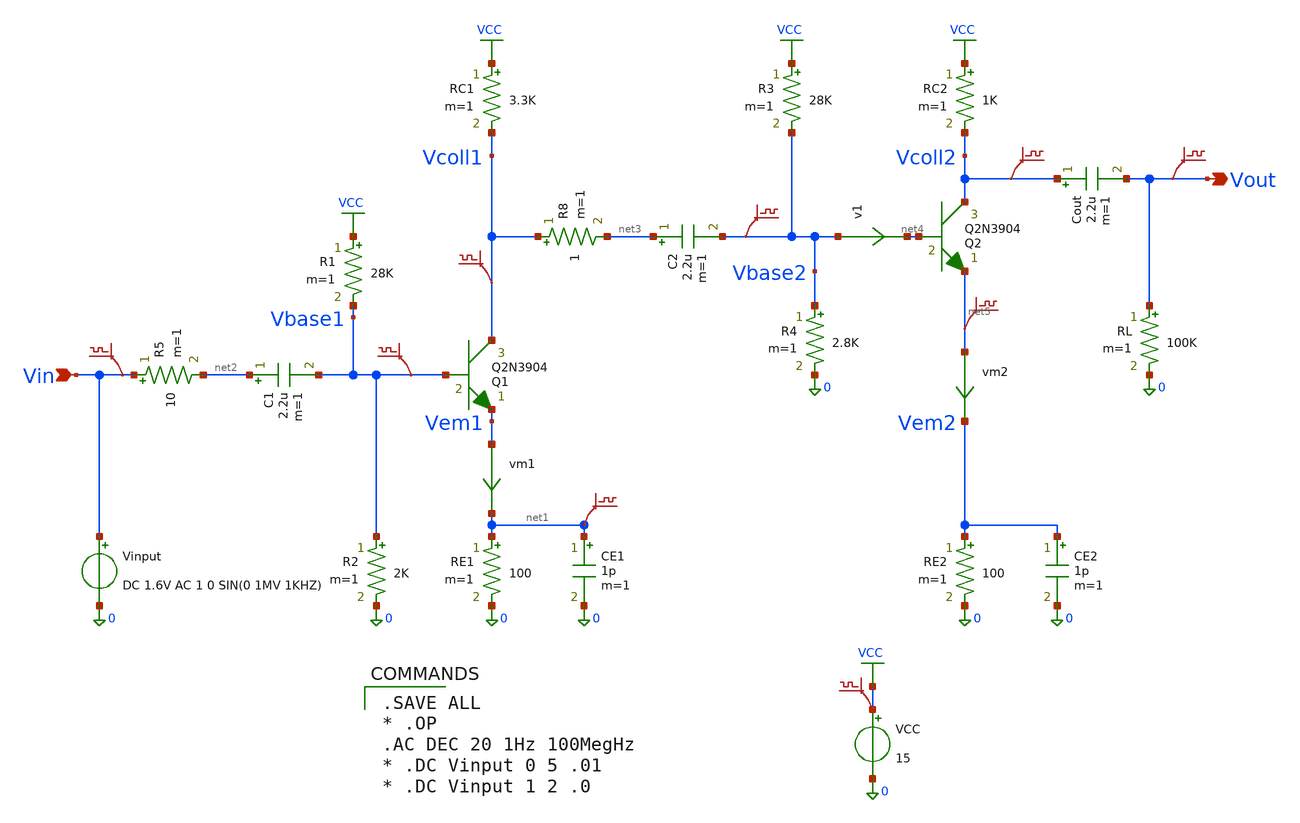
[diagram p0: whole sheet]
** sch_path: xschem_libraries_oa/examples/TwoStageAmp/schematic/TwoStageAmp.sch
* Copyright (C) 1998-2024 Stefan Frederik Schippers
* This program is free software; you can redistribute it and/or modify
* it under the terms of the GNU General Public License as published by
* the Free Software Foundation; either version 2 of the License, or
* (at your option) any later version.
* This program is distributed in the hope that it will be useful,
* but WITHOUT ANY WARRANTY; without even the implied warranty of
* MERCHANTABILITY or FITNESS FOR A PARTICULAR PURPOSE.  See the
* GNU General Public License for more details.
* You should have received a copy of the GNU General Public License
* along with this program; if not, write to the Free Software
**.subckt TwoStageAmp Vin Vout
*.ipin Vin
*.opin Vout
Vinput Vin 0 DC 1.6V AC 1 0 SIN(0 1MV 1KHZ)
R5 Vin net2 10 m=1
C1 net2 Vbase1 2.2u m=1
R1 VCC Vbase1 28K m=1
R2 Vbase1 0 2K m=1
Q1 Vcoll1 Vbase1 Vem1 Q2N3904 area=1 m=1
RE1 net1 0 100 m=1
CE1 net1 0 1p m=1
RC1 VCC Vcoll1 3.3K m=1
R8 Vcoll1 net3 1 m=1
C2 net3 Vbase2 2.2u m=1
R3 VCC Vbase2 28K m=1
R4 Vbase2 0 2.8K m=1
Q2 Vcoll2 net4 net5 Q2N3904 area=1 m=1
RC2 VCC Vcoll2 1K m=1
RE2 Vem2 0 100 m=1
CE2 Vem2 0 1p m=1
Cout Vcoll2 Vout 2.2u m=1
RL Vout 0 100K m=1
VCC VCC 0 15
.save v(vout)
.save v(vbase2)
.save v(net5)
.save v(vcoll1)
.save v(vbase1)
.save v(vin)
.save v(vcoll2)
vm2 net5 Vem2 0
.save i(vm2)
vm1 Vem1 net1 0
.save i(vm1)
.save v(net1)
.save v(vcc)
v1 Vbase2 net4 0
.save i(v1)
**** begin user architecture code

.model Q2N3904   NPN(Is=6.734f Xti=3 Eg=1.11 Vaf=74.03 Bf=416.4 Ne=1.259                Ise=6.734f
+ Ikf=66.78m Xtb=1.5 Br=.7371 Nc=2 Isc=0 Ikr=0 Rc=1                Cjc=3.638p Mjc=.3085 Vjc=.75 Fc=.5 Cje=4.493p
+ Mje=.2593 Vje=.75                Tr=239.5n Tf=301.2p Itf=.4 Vtf=4 Xtf=2 Rb=10)
*               Fairchild        pid=23          case=TO92
*               88-09-08 bam    creation




.SAVE ALL
* .OP
.AC DEC 20 1Hz 100MegHz
* .DC Vinput 0 5 .01
* .DC Vinput 1 2 .0


**** end user architecture code
**.ends
.GLOBAL VCC
.end
